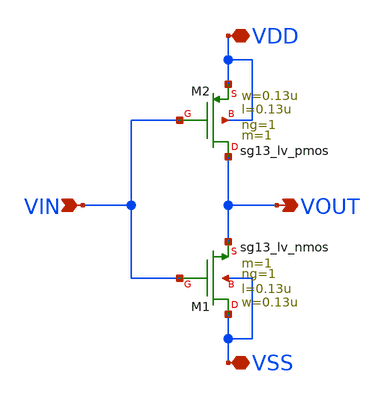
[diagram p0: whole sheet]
** sch_path: W2W-DAC/W2W_BOX/inv.sch
**.subckt inv VDD VSS VOUT VIN
*.iopin VDD
*.iopin VSS
*.opin VOUT
*.ipin VIN
XM1 VSS VIN VOUT VSS sg13_lv_nmos w=0.13u l=0.13u ng=1 m=1 mm_ok=1
XM2 VOUT VIN VDD VDD sg13_lv_pmos w=0.13u l=0.13u ng=1 m=1 mm_ok=1
**.ends
.end
